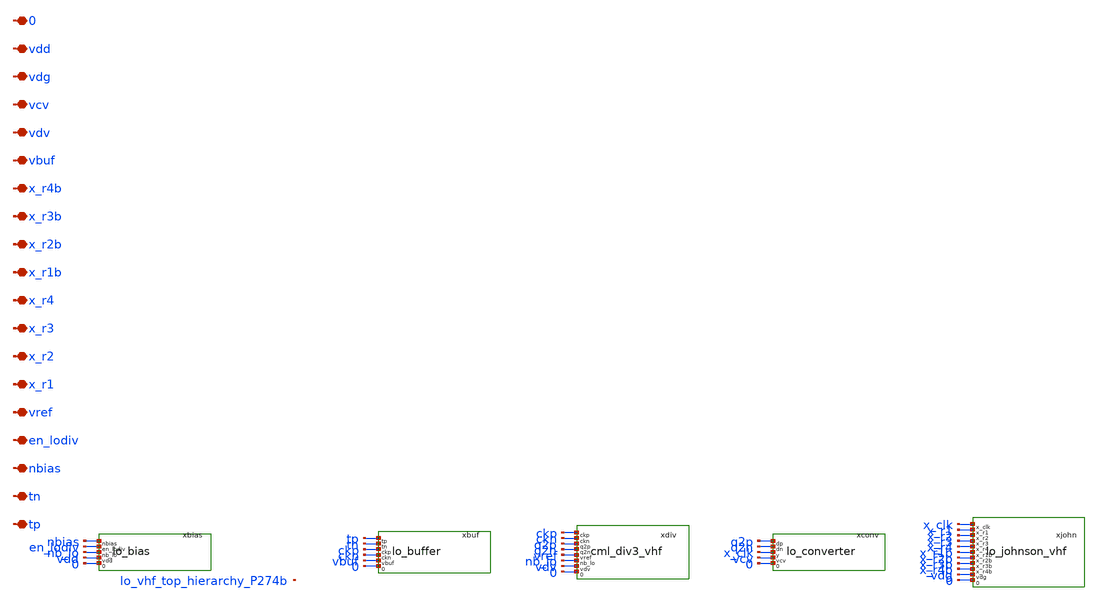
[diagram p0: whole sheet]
** sch_path: analog/lo/sch/lo_vhf_top.sch
**.subckt lo_vhf_top tp tn nbias en_lodiv vref x_r1 x_r2 x_r3 x_r4 x_r1b x_r2b x_r3b x_r4b vbuf vdv
*+ vcv vdg vdd 0
*.iopin tp
*.iopin tn
*.iopin nbias
*.iopin en_lodiv
*.iopin vref
*.iopin x_r1
*.iopin x_r2
*.iopin x_r3
*.iopin x_r4
*.iopin x_r1b
*.iopin x_r2b
*.iopin x_r3b
*.iopin x_r4b
*.iopin vbuf
*.iopin vdv
*.iopin vcv
*.iopin vdg
*.iopin vdd
*.iopin 0
xbias nbias en_lodiv nb_lo vdd 0 lo_bias
xbuf tp tn ckp ckn vbuf 0 lo_buffer
xdiv ckp ckn q2p q2n vref nb_lo vdv 0 cml_div3_vhf
xconv q2p q2n x_clk vcv 0 lo_converter
xjohn x_clk x_r1 x_r2 x_r3 x_r4 x_r1b x_r2b x_r3b x_r4b vdg 0 lo_johnson_vhf
**.ends

* expanding   symbol:  lo_bias.sym # of pins=5
** sym_path: analog/lo/sch/lo_bias.sym
** sch_path: analog/lo/sch/lo_bias.sch
.subckt lo_bias nbias en_lodiv nb_lo vdd 0
*.iopin nbias
*.iopin en_lodiv
*.iopin nb_lo
*.iopin vdd
*.iopin 0
Xxenb_p en_n en_lodiv vdd vdd sg13_lv_pmos w=1u l=0.13u ng=1 m=1 mm_ok=1
Xxenb_n en_n en_lodiv 0 0 sg13_lv_nmos w=0.5u l=0.13u ng=1 m=1 mm_ok=1
Xtgn nb_lo en_lodiv nbias 0 sg13_lv_nmos w=4u l=0.13u ng=1 m=1 mm_ok=1
Xtgp nb_lo en_n nbias vdd sg13_lv_pmos w=8u l=0.13u ng=1 m=1 mm_ok=1
Xmpd nb_lo en_n 0 0 sg13_lv_nmos w=2u l=0.13u ng=1 m=1 mm_ok=1
.ends


* expanding   symbol:  lo_buffer.sym # of pins=6
** sym_path: analog/lo/sch/lo_buffer.sym
** sch_path: analog/lo/sch/lo_buffer.sch
.subckt lo_buffer tp tn ckp ckn vbuf 0
*.iopin tp
*.iopin tn
*.iopin ckp
*.iopin ckn
*.iopin vbuf
*.iopin 0
ccp tp x_bip 100f m=1
rfp x_bip x_bop 50k m=1
Xxb1pp x_bop x_bip vbuf vbuf sg13_lv_pmos w=4u l=0.13u ng=1 m=1 mm_ok=1
Xxb1pn x_bop x_bip 0 0 sg13_lv_nmos w=2u l=0.13u ng=1 m=1 mm_ok=1
ccmp x_bop x_mip 50f m=1
rfmp x_mip x_bmp 50k m=1
Xxbmpp x_bmp x_mip vbuf vbuf sg13_lv_pmos w=6u l=0.13u ng=1 m=1 mm_ok=1
Xxbmpn x_bmp x_mip 0 0 sg13_lv_nmos w=3u l=0.13u ng=1 m=1 mm_ok=1
Xxb2pp ckp x_bmp vbuf vbuf sg13_lv_pmos w=8.0u l=0.13u ng=1 m=1 mm_ok=1
Xxb2pn ckp x_bmp 0 0 sg13_lv_nmos w=4.0u l=0.13u ng=1 m=1 mm_ok=1
ccn tn x_bin 100f m=1
rfn x_bin x_bon 50k m=1
Xxb1np x_bon x_bin vbuf vbuf sg13_lv_pmos w=4u l=0.13u ng=1 m=1 mm_ok=1
Xxb1nn x_bon x_bin 0 0 sg13_lv_nmos w=2u l=0.13u ng=1 m=1 mm_ok=1
ccmn x_bon x_min 50f m=1
rfmn x_min x_bmn 50k m=1
Xxbmnp x_bmn x_min vbuf vbuf sg13_lv_pmos w=6u l=0.13u ng=1 m=1 mm_ok=1
Xxbmnn x_bmn x_min 0 0 sg13_lv_nmos w=3u l=0.13u ng=1 m=1 mm_ok=1
Xxb2np ckn x_bmn vbuf vbuf sg13_lv_pmos w=8.0u l=0.13u ng=1 m=1 mm_ok=1
Xxb2nn ckn x_bmn 0 0 sg13_lv_nmos w=4.0u l=0.13u ng=1 m=1 mm_ok=1
Xxbxpp x_bon x_bop vbuf vbuf sg13_lv_pmos w=1u l=0.13u ng=1 m=1 mm_ok=1
Xxbxpn x_bon x_bop 0 0 sg13_lv_nmos w=0.5u l=0.13u ng=1 m=1 mm_ok=1
Xxbxnp x_bop x_bon vbuf vbuf sg13_lv_pmos w=1u l=0.13u ng=1 m=1 mm_ok=1
Xxbxnn x_bop x_bon 0 0 sg13_lv_nmos w=0.5u l=0.13u ng=1 m=1 mm_ok=1
Xxbopp ckn ckp vbuf vbuf sg13_lv_pmos w=2u l=0.13u ng=1 m=1 mm_ok=1
Xxbopn ckn ckp 0 0 sg13_lv_nmos w=1u l=0.13u ng=1 m=1 mm_ok=1
Xxbonp ckp ckn vbuf vbuf sg13_lv_pmos w=2u l=0.13u ng=1 m=1 mm_ok=1
Xxbonn ckp ckn 0 0 sg13_lv_nmos w=1u l=0.13u ng=1 m=1 mm_ok=1
.ends


* expanding   symbol:  cml_div3_vhf.sym # of pins=8
** sym_path: analog/lo/sch/cml_div3_vhf.sym
** sch_path: analog/lo/sch/cml_div3_vhf.sch
.subckt cml_div3_vhf ckp ckn q2p q2n vref nb_lo vdv 0
*.iopin ckp
*.iopin ckn
*.iopin q2p
*.iopin q2n
*.iopin vref
*.iopin nb_lo
*.iopin vdv
*.iopin 0
rgp vdv orp 1666.7 m=1
rgn vdv orn 1666.7 m=1
Xmga orn q1p tg 0 sg13_lv_nmos w=3.00u l=0.13u ng=1 m=1 mm_ok=1
Xmgb orn q2p tg 0 sg13_lv_nmos w=3.00u l=0.13u ng=1 m=1 mm_ok=1
Xmgr orp vref tg 0 sg13_lv_nmos w=3.00u l=0.13u ng=1 m=1 mm_ok=1
Xmtg tg nb_lo 0 0 sg13_lv_nmos w=6u l=0.13u ng=1 m=1 mm_ok=1
rlamp vdv map 1666.7 m=1
rlamn vdv man 1666.7 m=1
Xmam1 man orn s1am 0 sg13_lv_nmos w=3.00u l=0.13u ng=1 m=1 mm_ok=1
Xmam2 map orp s1am 0 sg13_lv_nmos w=3.00u l=0.13u ng=1 m=1 mm_ok=1
Xmam3 man map s2am 0 sg13_lv_nmos w=4.50u l=0.13u ng=1 m=1 mm_ok=1
Xmam4 map man s2am 0 sg13_lv_nmos w=4.50u l=0.13u ng=1 m=1 mm_ok=1
Xmam5 s1am ckp 0 0 sg13_lv_nmos w=3.00u l=0.13u ng=1 m=1 mm_ok=1
Xmam6 s2am ckn 0 0 sg13_lv_nmos w=3.00u l=0.13u ng=1 m=1 mm_ok=1
rlasp vdv q1p 1666.7 m=1
rlasn vdv q1n 1666.7 m=1
Xmas1 q1n map s1as 0 sg13_lv_nmos w=3.00u l=0.13u ng=1 m=1 mm_ok=1
Xmas2 q1p man s1as 0 sg13_lv_nmos w=3.00u l=0.13u ng=1 m=1 mm_ok=1
Xmas3 q1n q1p s2as 0 sg13_lv_nmos w=4.50u l=0.13u ng=1 m=1 mm_ok=1
Xmas4 q1p q1n s2as 0 sg13_lv_nmos w=4.50u l=0.13u ng=1 m=1 mm_ok=1
Xmas5 s1as ckn 0 0 sg13_lv_nmos w=3.00u l=0.13u ng=1 m=1 mm_ok=1
Xmas6 s2as ckp 0 0 sg13_lv_nmos w=3.00u l=0.13u ng=1 m=1 mm_ok=1
rlbmp vdv mbp 1666.7 m=1
rlbmn vdv mbn 1666.7 m=1
Xmbm1 mbn q1p s1bm 0 sg13_lv_nmos w=3.00u l=0.13u ng=1 m=1 mm_ok=1
Xmbm2 mbp q1n s1bm 0 sg13_lv_nmos w=3.00u l=0.13u ng=1 m=1 mm_ok=1
Xmbm3 mbn mbp s2bm 0 sg13_lv_nmos w=4.50u l=0.13u ng=1 m=1 mm_ok=1
Xmbm4 mbp mbn s2bm 0 sg13_lv_nmos w=4.50u l=0.13u ng=1 m=1 mm_ok=1
Xmbm5 s1bm ckp 0 0 sg13_lv_nmos w=3.00u l=0.13u ng=1 m=1 mm_ok=1
Xmbm6 s2bm ckn 0 0 sg13_lv_nmos w=3.00u l=0.13u ng=1 m=1 mm_ok=1
rlbsp vdv q2p 1666.7 m=1
rlbsn vdv q2n 1666.7 m=1
Xmbs1 q2n mbp s1bs 0 sg13_lv_nmos w=3.00u l=0.13u ng=1 m=1 mm_ok=1
Xmbs2 q2p mbn s1bs 0 sg13_lv_nmos w=3.00u l=0.13u ng=1 m=1 mm_ok=1
Xmbs3 q2n q2p s2bs 0 sg13_lv_nmos w=4.50u l=0.13u ng=1 m=1 mm_ok=1
Xmbs4 q2p q2n s2bs 0 sg13_lv_nmos w=4.50u l=0.13u ng=1 m=1 mm_ok=1
Xmbs5 s1bs ckn 0 0 sg13_lv_nmos w=3.00u l=0.13u ng=1 m=1 mm_ok=1
Xmbs6 s2bs ckp 0 0 sg13_lv_nmos w=3.00u l=0.13u ng=1 m=1 mm_ok=1
.ends


* expanding   symbol:  lo_converter.sym # of pins=5
** sym_path: analog/lo/sch/lo_converter.sym
** sch_path: analog/lo/sch/lo_converter.sch
.subckt lo_converter dp dn y vcv 0
*.iopin dp
*.iopin dn
*.iopin y
*.iopin vcv
*.iopin 0
ccap dp x_cip 50f m=1
rcap x_cip x_o2p 50k m=1
Xxcapp x_o2p x_cip vcv vcv sg13_lv_pmos w=4u l=0.13u ng=1 m=1 mm_ok=1
Xxcapn x_o2p x_cip 0 0 sg13_lv_nmos w=2u l=0.13u ng=1 m=1 mm_ok=1
ccan dn x_cin 50f m=1
rcan x_cin x_o2n 50k m=1
Xxcanp x_o2n x_cin vcv vcv sg13_lv_pmos w=4u l=0.13u ng=1 m=1 mm_ok=1
Xxcann x_o2n x_cin 0 0 sg13_lv_nmos w=2u l=0.13u ng=1 m=1 mm_ok=1
Xxcxpp x_o2n x_o2p vcv vcv sg13_lv_pmos w=1u l=0.13u ng=1 m=1 mm_ok=1
Xxcxpn x_o2n x_o2p 0 0 sg13_lv_nmos w=0.5u l=0.13u ng=1 m=1 mm_ok=1
Xxcxnp x_o2p x_o2n vcv vcv sg13_lv_pmos w=1u l=0.13u ng=1 m=1 mm_ok=1
Xxcxnn x_o2p x_o2n 0 0 sg13_lv_nmos w=0.5u l=0.13u ng=1 m=1 mm_ok=1
ccb x_o2p x_cbi 50f m=1
rcb x_cbi x_cy 50k m=1
Xxcbp x_cy x_cbi vcv vcv sg13_lv_pmos w=4u l=0.13u ng=1 m=1 mm_ok=1
Xxcbn x_cy x_cbi 0 0 sg13_lv_nmos w=2u l=0.13u ng=1 m=1 mm_ok=1
Xxcv3p x_cz x_cy vcv vcv sg13_lv_pmos w=6.0u l=0.13u ng=1 m=1 mm_ok=1
Xxcv3n x_cz x_cy 0 0 sg13_lv_nmos w=3.0u l=0.13u ng=1 m=1 mm_ok=1
Xxcv4p y x_cz vcv vcv sg13_lv_pmos w=18.0u l=0.13u ng=1 m=1 mm_ok=1
Xxcv4n y x_cz 0 0 sg13_lv_nmos w=9.0u l=0.13u ng=1 m=1 mm_ok=1
.ends


* expanding   symbol:  lo_johnson_vhf.sym # of pins=11
** sym_path: analog/lo/sch/lo_johnson_vhf.sym
** sch_path: analog/lo/sch/lo_johnson_vhf.sch
.subckt lo_johnson_vhf x_clk x_r1 x_r2 x_r3 x_r4 x_r1b x_r2b x_r3b x_r4b vdg 0
*.iopin x_clk
*.iopin x_r1
*.iopin x_r2
*.iopin x_r3
*.iopin x_r4
*.iopin x_r1b
*.iopin x_r2b
*.iopin x_r3b
*.iopin x_r4b
*.iopin vdg
*.iopin 0
Xxf1p1 x_f1_x1 x_q4 vdg vdg sg13_lv_pmos w=2u l=0.13u ng=1 m=1 mm_ok=1
Xxf1p2 x_f1_a x_clk x_f1_x1 vdg sg13_lv_pmos w=2u l=0.13u ng=1 m=1 mm_ok=1
Xxf1n1 x_f1_a x_q4 0 0 sg13_lv_nmos w=1u l=0.13u ng=1 m=1 mm_ok=1
Xxf1p3 x_f1_b x_clk vdg vdg sg13_lv_pmos w=2u l=0.13u ng=1 m=1 mm_ok=1
Xxf1n2 x_f1_b x_f1_a x_f1_x2 0 sg13_lv_nmos w=1u l=0.13u ng=1 m=1 mm_ok=1
Xxf1n3 x_f1_x2 x_clk 0 0 sg13_lv_nmos w=1u l=0.13u ng=1 m=1 mm_ok=1
Xxf1p4 x_q1 x_f1_b vdg vdg sg13_lv_pmos w=2u l=0.13u ng=1 m=1 mm_ok=1
Xxf1n4 x_q1 x_clk x_f1_x3 0 sg13_lv_nmos w=1u l=0.13u ng=1 m=1 mm_ok=1
Xxf1n5 x_f1_x3 x_f1_b 0 0 sg13_lv_nmos w=1u l=0.13u ng=1 m=1 mm_ok=1
Xxi2p x_d2 x_q1 vdg vdg sg13_lv_pmos w=1.0u l=0.13u ng=1 m=1 mm_ok=1
Xxi2n x_d2 x_q1 0 0 sg13_lv_nmos w=0.5u l=0.13u ng=1 m=1 mm_ok=1
Xxf2p1 x_f2_x1 x_d2 vdg vdg sg13_lv_pmos w=2u l=0.13u ng=1 m=1 mm_ok=1
Xxf2p2 x_f2_a x_clk x_f2_x1 vdg sg13_lv_pmos w=2u l=0.13u ng=1 m=1 mm_ok=1
Xxf2n1 x_f2_a x_d2 0 0 sg13_lv_nmos w=1u l=0.13u ng=1 m=1 mm_ok=1
Xxf2p3 x_f2_b x_clk vdg vdg sg13_lv_pmos w=2u l=0.13u ng=1 m=1 mm_ok=1
Xxf2n2 x_f2_b x_f2_a x_f2_x2 0 sg13_lv_nmos w=1u l=0.13u ng=1 m=1 mm_ok=1
Xxf2n3 x_f2_x2 x_clk 0 0 sg13_lv_nmos w=1u l=0.13u ng=1 m=1 mm_ok=1
Xxf2p4 x_q2 x_f2_b vdg vdg sg13_lv_pmos w=2u l=0.13u ng=1 m=1 mm_ok=1
Xxf2n4 x_q2 x_clk x_f2_x3 0 sg13_lv_nmos w=1u l=0.13u ng=1 m=1 mm_ok=1
Xxf2n5 x_f2_x3 x_f2_b 0 0 sg13_lv_nmos w=1u l=0.13u ng=1 m=1 mm_ok=1
Xxi3p x_d3 x_q2 vdg vdg sg13_lv_pmos w=1.0u l=0.13u ng=1 m=1 mm_ok=1
Xxi3n x_d3 x_q2 0 0 sg13_lv_nmos w=0.5u l=0.13u ng=1 m=1 mm_ok=1
Xxf3p1 x_f3_x1 x_d3 vdg vdg sg13_lv_pmos w=2u l=0.13u ng=1 m=1 mm_ok=1
Xxf3p2 x_f3_a x_clk x_f3_x1 vdg sg13_lv_pmos w=2u l=0.13u ng=1 m=1 mm_ok=1
Xxf3n1 x_f3_a x_d3 0 0 sg13_lv_nmos w=1u l=0.13u ng=1 m=1 mm_ok=1
Xxf3p3 x_f3_b x_clk vdg vdg sg13_lv_pmos w=2u l=0.13u ng=1 m=1 mm_ok=1
Xxf3n2 x_f3_b x_f3_a x_f3_x2 0 sg13_lv_nmos w=1u l=0.13u ng=1 m=1 mm_ok=1
Xxf3n3 x_f3_x2 x_clk 0 0 sg13_lv_nmos w=1u l=0.13u ng=1 m=1 mm_ok=1
Xxf3p4 x_q3 x_f3_b vdg vdg sg13_lv_pmos w=2u l=0.13u ng=1 m=1 mm_ok=1
Xxf3n4 x_q3 x_clk x_f3_x3 0 sg13_lv_nmos w=1u l=0.13u ng=1 m=1 mm_ok=1
Xxf3n5 x_f3_x3 x_f3_b 0 0 sg13_lv_nmos w=1u l=0.13u ng=1 m=1 mm_ok=1
Xxi4p x_d4 x_q3 vdg vdg sg13_lv_pmos w=1.0u l=0.13u ng=1 m=1 mm_ok=1
Xxi4n x_d4 x_q3 0 0 sg13_lv_nmos w=0.5u l=0.13u ng=1 m=1 mm_ok=1
Xxf4p1 x_f4_x1 x_d4 vdg vdg sg13_lv_pmos w=2u l=0.13u ng=1 m=1 mm_ok=1
Xxf4p2 x_f4_a x_clk x_f4_x1 vdg sg13_lv_pmos w=2u l=0.13u ng=1 m=1 mm_ok=1
Xxf4n1 x_f4_a x_d4 0 0 sg13_lv_nmos w=1u l=0.13u ng=1 m=1 mm_ok=1
Xxf4p3 x_f4_b x_clk vdg vdg sg13_lv_pmos w=2u l=0.13u ng=1 m=1 mm_ok=1
Xxf4n2 x_f4_b x_f4_a x_f4_x2 0 sg13_lv_nmos w=1u l=0.13u ng=1 m=1 mm_ok=1
Xxf4n3 x_f4_x2 x_clk 0 0 sg13_lv_nmos w=1u l=0.13u ng=1 m=1 mm_ok=1
Xxf4p4 x_q4 x_f4_b vdg vdg sg13_lv_pmos w=2u l=0.13u ng=1 m=1 mm_ok=1
Xxf4n4 x_q4 x_clk x_f4_x3 0 sg13_lv_nmos w=1u l=0.13u ng=1 m=1 mm_ok=1
Xxf4n5 x_f4_x3 x_f4_b 0 0 sg13_lv_nmos w=1u l=0.13u ng=1 m=1 mm_ok=1
Xxo1p x_q1b x_q1 vdg vdg sg13_lv_pmos w=1.0u l=0.13u ng=1 m=1 mm_ok=1
Xxo1n x_q1b x_q1 0 0 sg13_lv_nmos w=0.5u l=0.13u ng=1 m=1 mm_ok=1
Xxr1ap1 x_r1a_x1 x_q1b vdg vdg sg13_lv_pmos w=2u l=0.13u ng=1 m=1 mm_ok=1
Xxr1ap2 x_r1a_a x_clk x_r1a_x1 vdg sg13_lv_pmos w=2u l=0.13u ng=1 m=1 mm_ok=1
Xxr1an1 x_r1a_a x_q1b 0 0 sg13_lv_nmos w=1u l=0.13u ng=1 m=1 mm_ok=1
Xxr1ap3 x_r1a_b x_clk vdg vdg sg13_lv_pmos w=2u l=0.13u ng=1 m=1 mm_ok=1
Xxr1an2 x_r1a_b x_r1a_a x_r1a_x2 0 sg13_lv_nmos w=1u l=0.13u ng=1 m=1 mm_ok=1
Xxr1an3 x_r1a_x2 x_clk 0 0 sg13_lv_nmos w=1u l=0.13u ng=1 m=1 mm_ok=1
Xxr1ap4 x_r1 x_r1a_b vdg vdg sg13_lv_pmos w=2u l=0.13u ng=1 m=1 mm_ok=1
Xxr1an4 x_r1 x_clk x_r1a_x3 0 sg13_lv_nmos w=1u l=0.13u ng=1 m=1 mm_ok=1
Xxr1an5 x_r1a_x3 x_r1a_b 0 0 sg13_lv_nmos w=1u l=0.13u ng=1 m=1 mm_ok=1
Xxr1bp1 x_r1b_x1 x_q1 vdg vdg sg13_lv_pmos w=2u l=0.13u ng=1 m=1 mm_ok=1
Xxr1bp2 x_r1b_a x_clk x_r1b_x1 vdg sg13_lv_pmos w=2u l=0.13u ng=1 m=1 mm_ok=1
Xxr1bn1 x_r1b_a x_q1 0 0 sg13_lv_nmos w=1u l=0.13u ng=1 m=1 mm_ok=1
Xxr1bp3 x_r1b_b x_clk vdg vdg sg13_lv_pmos w=2u l=0.13u ng=1 m=1 mm_ok=1
Xxr1bn2 x_r1b_b x_r1b_a x_r1b_x2 0 sg13_lv_nmos w=1u l=0.13u ng=1 m=1 mm_ok=1
Xxr1bn3 x_r1b_x2 x_clk 0 0 sg13_lv_nmos w=1u l=0.13u ng=1 m=1 mm_ok=1
Xxr1bp4 x_r1b x_r1b_b vdg vdg sg13_lv_pmos w=2u l=0.13u ng=1 m=1 mm_ok=1
Xxr1bn4 x_r1b x_clk x_r1b_x3 0 sg13_lv_nmos w=1u l=0.13u ng=1 m=1 mm_ok=1
Xxr1bn5 x_r1b_x3 x_r1b_b 0 0 sg13_lv_nmos w=1u l=0.13u ng=1 m=1 mm_ok=1
cr1 x_r1 0 10f m=1
crb1 x_r1b 0 10f m=1
Xxo2p x_q2b x_q2 vdg vdg sg13_lv_pmos w=1.0u l=0.13u ng=1 m=1 mm_ok=1
Xxo2n x_q2b x_q2 0 0 sg13_lv_nmos w=0.5u l=0.13u ng=1 m=1 mm_ok=1
Xxr2ap1 x_r2a_x1 x_q2b vdg vdg sg13_lv_pmos w=2u l=0.13u ng=1 m=1 mm_ok=1
Xxr2ap2 x_r2a_a x_clk x_r2a_x1 vdg sg13_lv_pmos w=2u l=0.13u ng=1 m=1 mm_ok=1
Xxr2an1 x_r2a_a x_q2b 0 0 sg13_lv_nmos w=1u l=0.13u ng=1 m=1 mm_ok=1
Xxr2ap3 x_r2a_b x_clk vdg vdg sg13_lv_pmos w=2u l=0.13u ng=1 m=1 mm_ok=1
Xxr2an2 x_r2a_b x_r2a_a x_r2a_x2 0 sg13_lv_nmos w=1u l=0.13u ng=1 m=1 mm_ok=1
Xxr2an3 x_r2a_x2 x_clk 0 0 sg13_lv_nmos w=1u l=0.13u ng=1 m=1 mm_ok=1
Xxr2ap4 x_r2 x_r2a_b vdg vdg sg13_lv_pmos w=2u l=0.13u ng=1 m=1 mm_ok=1
Xxr2an4 x_r2 x_clk x_r2a_x3 0 sg13_lv_nmos w=1u l=0.13u ng=1 m=1 mm_ok=1
Xxr2an5 x_r2a_x3 x_r2a_b 0 0 sg13_lv_nmos w=1u l=0.13u ng=1 m=1 mm_ok=1
Xxr2bp1 x_r2b_x1 x_q2 vdg vdg sg13_lv_pmos w=2u l=0.13u ng=1 m=1 mm_ok=1
Xxr2bp2 x_r2b_a x_clk x_r2b_x1 vdg sg13_lv_pmos w=2u l=0.13u ng=1 m=1 mm_ok=1
Xxr2bn1 x_r2b_a x_q2 0 0 sg13_lv_nmos w=1u l=0.13u ng=1 m=1 mm_ok=1
Xxr2bp3 x_r2b_b x_clk vdg vdg sg13_lv_pmos w=2u l=0.13u ng=1 m=1 mm_ok=1
Xxr2bn2 x_r2b_b x_r2b_a x_r2b_x2 0 sg13_lv_nmos w=1u l=0.13u ng=1 m=1 mm_ok=1
Xxr2bn3 x_r2b_x2 x_clk 0 0 sg13_lv_nmos w=1u l=0.13u ng=1 m=1 mm_ok=1
Xxr2bp4 x_r2b x_r2b_b vdg vdg sg13_lv_pmos w=2u l=0.13u ng=1 m=1 mm_ok=1
Xxr2bn4 x_r2b x_clk x_r2b_x3 0 sg13_lv_nmos w=1u l=0.13u ng=1 m=1 mm_ok=1
Xxr2bn5 x_r2b_x3 x_r2b_b 0 0 sg13_lv_nmos w=1u l=0.13u ng=1 m=1 mm_ok=1
cr2 x_r2 0 10f m=1
crb2 x_r2b 0 10f m=1
Xxo3p x_q3b x_q3 vdg vdg sg13_lv_pmos w=1.0u l=0.13u ng=1 m=1 mm_ok=1
Xxo3n x_q3b x_q3 0 0 sg13_lv_nmos w=0.5u l=0.13u ng=1 m=1 mm_ok=1
Xxr3ap1 x_r3a_x1 x_q3b vdg vdg sg13_lv_pmos w=2u l=0.13u ng=1 m=1 mm_ok=1
Xxr3ap2 x_r3a_a x_clk x_r3a_x1 vdg sg13_lv_pmos w=2u l=0.13u ng=1 m=1 mm_ok=1
Xxr3an1 x_r3a_a x_q3b 0 0 sg13_lv_nmos w=1u l=0.13u ng=1 m=1 mm_ok=1
Xxr3ap3 x_r3a_b x_clk vdg vdg sg13_lv_pmos w=2u l=0.13u ng=1 m=1 mm_ok=1
Xxr3an2 x_r3a_b x_r3a_a x_r3a_x2 0 sg13_lv_nmos w=1u l=0.13u ng=1 m=1 mm_ok=1
Xxr3an3 x_r3a_x2 x_clk 0 0 sg13_lv_nmos w=1u l=0.13u ng=1 m=1 mm_ok=1
Xxr3ap4 x_r3 x_r3a_b vdg vdg sg13_lv_pmos w=2u l=0.13u ng=1 m=1 mm_ok=1
Xxr3an4 x_r3 x_clk x_r3a_x3 0 sg13_lv_nmos w=1u l=0.13u ng=1 m=1 mm_ok=1
Xxr3an5 x_r3a_x3 x_r3a_b 0 0 sg13_lv_nmos w=1u l=0.13u ng=1 m=1 mm_ok=1
Xxr3bp1 x_r3b_x1 x_q3 vdg vdg sg13_lv_pmos w=2u l=0.13u ng=1 m=1 mm_ok=1
Xxr3bp2 x_r3b_a x_clk x_r3b_x1 vdg sg13_lv_pmos w=2u l=0.13u ng=1 m=1 mm_ok=1
Xxr3bn1 x_r3b_a x_q3 0 0 sg13_lv_nmos w=1u l=0.13u ng=1 m=1 mm_ok=1
Xxr3bp3 x_r3b_b x_clk vdg vdg sg13_lv_pmos w=2u l=0.13u ng=1 m=1 mm_ok=1
Xxr3bn2 x_r3b_b x_r3b_a x_r3b_x2 0 sg13_lv_nmos w=1u l=0.13u ng=1 m=1 mm_ok=1
Xxr3bn3 x_r3b_x2 x_clk 0 0 sg13_lv_nmos w=1u l=0.13u ng=1 m=1 mm_ok=1
Xxr3bp4 x_r3b x_r3b_b vdg vdg sg13_lv_pmos w=2u l=0.13u ng=1 m=1 mm_ok=1
Xxr3bn4 x_r3b x_clk x_r3b_x3 0 sg13_lv_nmos w=1u l=0.13u ng=1 m=1 mm_ok=1
Xxr3bn5 x_r3b_x3 x_r3b_b 0 0 sg13_lv_nmos w=1u l=0.13u ng=1 m=1 mm_ok=1
cr3 x_r3 0 10f m=1
crb3 x_r3b 0 10f m=1
Xxo4p x_q4b x_q4 vdg vdg sg13_lv_pmos w=1.0u l=0.13u ng=1 m=1 mm_ok=1
Xxo4n x_q4b x_q4 0 0 sg13_lv_nmos w=0.5u l=0.13u ng=1 m=1 mm_ok=1
Xxr4ap1 x_r4a_x1 x_q4b vdg vdg sg13_lv_pmos w=2u l=0.13u ng=1 m=1 mm_ok=1
Xxr4ap2 x_r4a_a x_clk x_r4a_x1 vdg sg13_lv_pmos w=2u l=0.13u ng=1 m=1 mm_ok=1
Xxr4an1 x_r4a_a x_q4b 0 0 sg13_lv_nmos w=1u l=0.13u ng=1 m=1 mm_ok=1
Xxr4ap3 x_r4a_b x_clk vdg vdg sg13_lv_pmos w=2u l=0.13u ng=1 m=1 mm_ok=1
Xxr4an2 x_r4a_b x_r4a_a x_r4a_x2 0 sg13_lv_nmos w=1u l=0.13u ng=1 m=1 mm_ok=1
Xxr4an3 x_r4a_x2 x_clk 0 0 sg13_lv_nmos w=1u l=0.13u ng=1 m=1 mm_ok=1
Xxr4ap4 x_r4 x_r4a_b vdg vdg sg13_lv_pmos w=2u l=0.13u ng=1 m=1 mm_ok=1
Xxr4an4 x_r4 x_clk x_r4a_x3 0 sg13_lv_nmos w=1u l=0.13u ng=1 m=1 mm_ok=1
Xxr4an5 x_r4a_x3 x_r4a_b 0 0 sg13_lv_nmos w=1u l=0.13u ng=1 m=1 mm_ok=1
Xxr4bp1 x_r4b_x1 x_q4 vdg vdg sg13_lv_pmos w=2u l=0.13u ng=1 m=1 mm_ok=1
Xxr4bp2 x_r4b_a x_clk x_r4b_x1 vdg sg13_lv_pmos w=2u l=0.13u ng=1 m=1 mm_ok=1
Xxr4bn1 x_r4b_a x_q4 0 0 sg13_lv_nmos w=1u l=0.13u ng=1 m=1 mm_ok=1
Xxr4bp3 x_r4b_b x_clk vdg vdg sg13_lv_pmos w=2u l=0.13u ng=1 m=1 mm_ok=1
Xxr4bn2 x_r4b_b x_r4b_a x_r4b_x2 0 sg13_lv_nmos w=1u l=0.13u ng=1 m=1 mm_ok=1
Xxr4bn3 x_r4b_x2 x_clk 0 0 sg13_lv_nmos w=1u l=0.13u ng=1 m=1 mm_ok=1
Xxr4bp4 x_r4b x_r4b_b vdg vdg sg13_lv_pmos w=2u l=0.13u ng=1 m=1 mm_ok=1
Xxr4bn4 x_r4b x_clk x_r4b_x3 0 sg13_lv_nmos w=1u l=0.13u ng=1 m=1 mm_ok=1
Xxr4bn5 x_r4b_x3 x_r4b_b 0 0 sg13_lv_nmos w=1u l=0.13u ng=1 m=1 mm_ok=1
cr4 x_r4 0 10f m=1
crb4 x_r4b 0 10f m=1
Xxf1kq1p x_f1_kq x_q1 vdg vdg sg13_lv_pmos w=0.3u l=0.13u ng=1 m=1 mm_ok=1
Xxf1kq1n x_f1_kq x_q1 0 0 sg13_lv_nmos w=0.15u l=0.13u ng=1 m=1 mm_ok=1
Xxf1kq2p x_q1 x_f1_kq vdg vdg sg13_lv_pmos w=0.3u l=0.13u ng=1 m=1 mm_ok=1
Xxf1kq2n x_q1 x_f1_kq 0 0 sg13_lv_nmos w=0.15u l=0.13u ng=1 m=1 mm_ok=1
rkf11 x_f1_a 0 100Meg m=1
rkf12 x_f1_b 0 100Meg m=1
Xxf2kq1p x_f2_kq x_q2 vdg vdg sg13_lv_pmos w=0.3u l=0.13u ng=1 m=1 mm_ok=1
Xxf2kq1n x_f2_kq x_q2 0 0 sg13_lv_nmos w=0.15u l=0.13u ng=1 m=1 mm_ok=1
Xxf2kq2p x_q2 x_f2_kq vdg vdg sg13_lv_pmos w=0.3u l=0.13u ng=1 m=1 mm_ok=1
Xxf2kq2n x_q2 x_f2_kq 0 0 sg13_lv_nmos w=0.15u l=0.13u ng=1 m=1 mm_ok=1
rkf21 x_f2_a 0 100Meg m=1
rkf22 x_f2_b 0 100Meg m=1
Xxf3kq1p x_f3_kq x_q3 vdg vdg sg13_lv_pmos w=0.3u l=0.13u ng=1 m=1 mm_ok=1
Xxf3kq1n x_f3_kq x_q3 0 0 sg13_lv_nmos w=0.15u l=0.13u ng=1 m=1 mm_ok=1
Xxf3kq2p x_q3 x_f3_kq vdg vdg sg13_lv_pmos w=0.3u l=0.13u ng=1 m=1 mm_ok=1
Xxf3kq2n x_q3 x_f3_kq 0 0 sg13_lv_nmos w=0.15u l=0.13u ng=1 m=1 mm_ok=1
rkf31 x_f3_a 0 100Meg m=1
rkf32 x_f3_b 0 100Meg m=1
Xxf4kq1p x_f4_kq x_q4 vdg vdg sg13_lv_pmos w=0.3u l=0.13u ng=1 m=1 mm_ok=1
Xxf4kq1n x_f4_kq x_q4 0 0 sg13_lv_nmos w=0.15u l=0.13u ng=1 m=1 mm_ok=1
Xxf4kq2p x_q4 x_f4_kq vdg vdg sg13_lv_pmos w=0.3u l=0.13u ng=1 m=1 mm_ok=1
Xxf4kq2n x_q4 x_f4_kq 0 0 sg13_lv_nmos w=0.15u l=0.13u ng=1 m=1 mm_ok=1
rkf41 x_f4_a 0 100Meg m=1
rkf42 x_f4_b 0 100Meg m=1
Xxr1akq1p x_r1a_kq x_r1 vdg vdg sg13_lv_pmos w=0.3u l=0.13u ng=1 m=1 mm_ok=1
Xxr1akq1n x_r1a_kq x_r1 0 0 sg13_lv_nmos w=0.15u l=0.13u ng=1 m=1 mm_ok=1
Xxr1akq2p x_r1 x_r1a_kq vdg vdg sg13_lv_pmos w=0.3u l=0.13u ng=1 m=1 mm_ok=1
Xxr1akq2n x_r1 x_r1a_kq 0 0 sg13_lv_nmos w=0.15u l=0.13u ng=1 m=1 mm_ok=1
rkr1a1 x_r1a_a 0 100Meg m=1
rkr1a2 x_r1a_b 0 100Meg m=1
Xxr1bkq1p x_r1b_kq x_r1b vdg vdg sg13_lv_pmos w=0.3u l=0.13u ng=1 m=1 mm_ok=1
Xxr1bkq1n x_r1b_kq x_r1b 0 0 sg13_lv_nmos w=0.15u l=0.13u ng=1 m=1 mm_ok=1
Xxr1bkq2p x_r1b x_r1b_kq vdg vdg sg13_lv_pmos w=0.3u l=0.13u ng=1 m=1 mm_ok=1
Xxr1bkq2n x_r1b x_r1b_kq 0 0 sg13_lv_nmos w=0.15u l=0.13u ng=1 m=1 mm_ok=1
rkr1b1 x_r1b_a 0 100Meg m=1
rkr1b2 x_r1b_b 0 100Meg m=1
Xxr2akq1p x_r2a_kq x_r2 vdg vdg sg13_lv_pmos w=0.3u l=0.13u ng=1 m=1 mm_ok=1
Xxr2akq1n x_r2a_kq x_r2 0 0 sg13_lv_nmos w=0.15u l=0.13u ng=1 m=1 mm_ok=1
Xxr2akq2p x_r2 x_r2a_kq vdg vdg sg13_lv_pmos w=0.3u l=0.13u ng=1 m=1 mm_ok=1
Xxr2akq2n x_r2 x_r2a_kq 0 0 sg13_lv_nmos w=0.15u l=0.13u ng=1 m=1 mm_ok=1
rkr2a1 x_r2a_a 0 100Meg m=1
rkr2a2 x_r2a_b 0 100Meg m=1
Xxr2bkq1p x_r2b_kq x_r2b vdg vdg sg13_lv_pmos w=0.3u l=0.13u ng=1 m=1 mm_ok=1
Xxr2bkq1n x_r2b_kq x_r2b 0 0 sg13_lv_nmos w=0.15u l=0.13u ng=1 m=1 mm_ok=1
Xxr2bkq2p x_r2b x_r2b_kq vdg vdg sg13_lv_pmos w=0.3u l=0.13u ng=1 m=1 mm_ok=1
Xxr2bkq2n x_r2b x_r2b_kq 0 0 sg13_lv_nmos w=0.15u l=0.13u ng=1 m=1 mm_ok=1
rkr2b1 x_r2b_a 0 100Meg m=1
rkr2b2 x_r2b_b 0 100Meg m=1
Xxr3akq1p x_r3a_kq x_r3 vdg vdg sg13_lv_pmos w=0.3u l=0.13u ng=1 m=1 mm_ok=1
Xxr3akq1n x_r3a_kq x_r3 0 0 sg13_lv_nmos w=0.15u l=0.13u ng=1 m=1 mm_ok=1
Xxr3akq2p x_r3 x_r3a_kq vdg vdg sg13_lv_pmos w=0.3u l=0.13u ng=1 m=1 mm_ok=1
Xxr3akq2n x_r3 x_r3a_kq 0 0 sg13_lv_nmos w=0.15u l=0.13u ng=1 m=1 mm_ok=1
rkr3a1 x_r3a_a 0 100Meg m=1
rkr3a2 x_r3a_b 0 100Meg m=1
Xxr3bkq1p x_r3b_kq x_r3b vdg vdg sg13_lv_pmos w=0.3u l=0.13u ng=1 m=1 mm_ok=1
Xxr3bkq1n x_r3b_kq x_r3b 0 0 sg13_lv_nmos w=0.15u l=0.13u ng=1 m=1 mm_ok=1
Xxr3bkq2p x_r3b x_r3b_kq vdg vdg sg13_lv_pmos w=0.3u l=0.13u ng=1 m=1 mm_ok=1
Xxr3bkq2n x_r3b x_r3b_kq 0 0 sg13_lv_nmos w=0.15u l=0.13u ng=1 m=1 mm_ok=1
rkr3b1 x_r3b_a 0 100Meg m=1
rkr3b2 x_r3b_b 0 100Meg m=1
Xxr4akq1p x_r4a_kq x_r4 vdg vdg sg13_lv_pmos w=0.3u l=0.13u ng=1 m=1 mm_ok=1
Xxr4akq1n x_r4a_kq x_r4 0 0 sg13_lv_nmos w=0.15u l=0.13u ng=1 m=1 mm_ok=1
Xxr4akq2p x_r4 x_r4a_kq vdg vdg sg13_lv_pmos w=0.3u l=0.13u ng=1 m=1 mm_ok=1
Xxr4akq2n x_r4 x_r4a_kq 0 0 sg13_lv_nmos w=0.15u l=0.13u ng=1 m=1 mm_ok=1
rkr4a1 x_r4a_a 0 100Meg m=1
rkr4a2 x_r4a_b 0 100Meg m=1
Xxr4bkq1p x_r4b_kq x_r4b vdg vdg sg13_lv_pmos w=0.3u l=0.13u ng=1 m=1 mm_ok=1
Xxr4bkq1n x_r4b_kq x_r4b 0 0 sg13_lv_nmos w=0.15u l=0.13u ng=1 m=1 mm_ok=1
Xxr4bkq2p x_r4b x_r4b_kq vdg vdg sg13_lv_pmos w=0.3u l=0.13u ng=1 m=1 mm_ok=1
Xxr4bkq2n x_r4b x_r4b_kq 0 0 sg13_lv_nmos w=0.15u l=0.13u ng=1 m=1 mm_ok=1
rkr4b1 x_r4b_a 0 100Meg m=1
rkr4b2 x_r4b_b 0 100Meg m=1
.ends

.end
